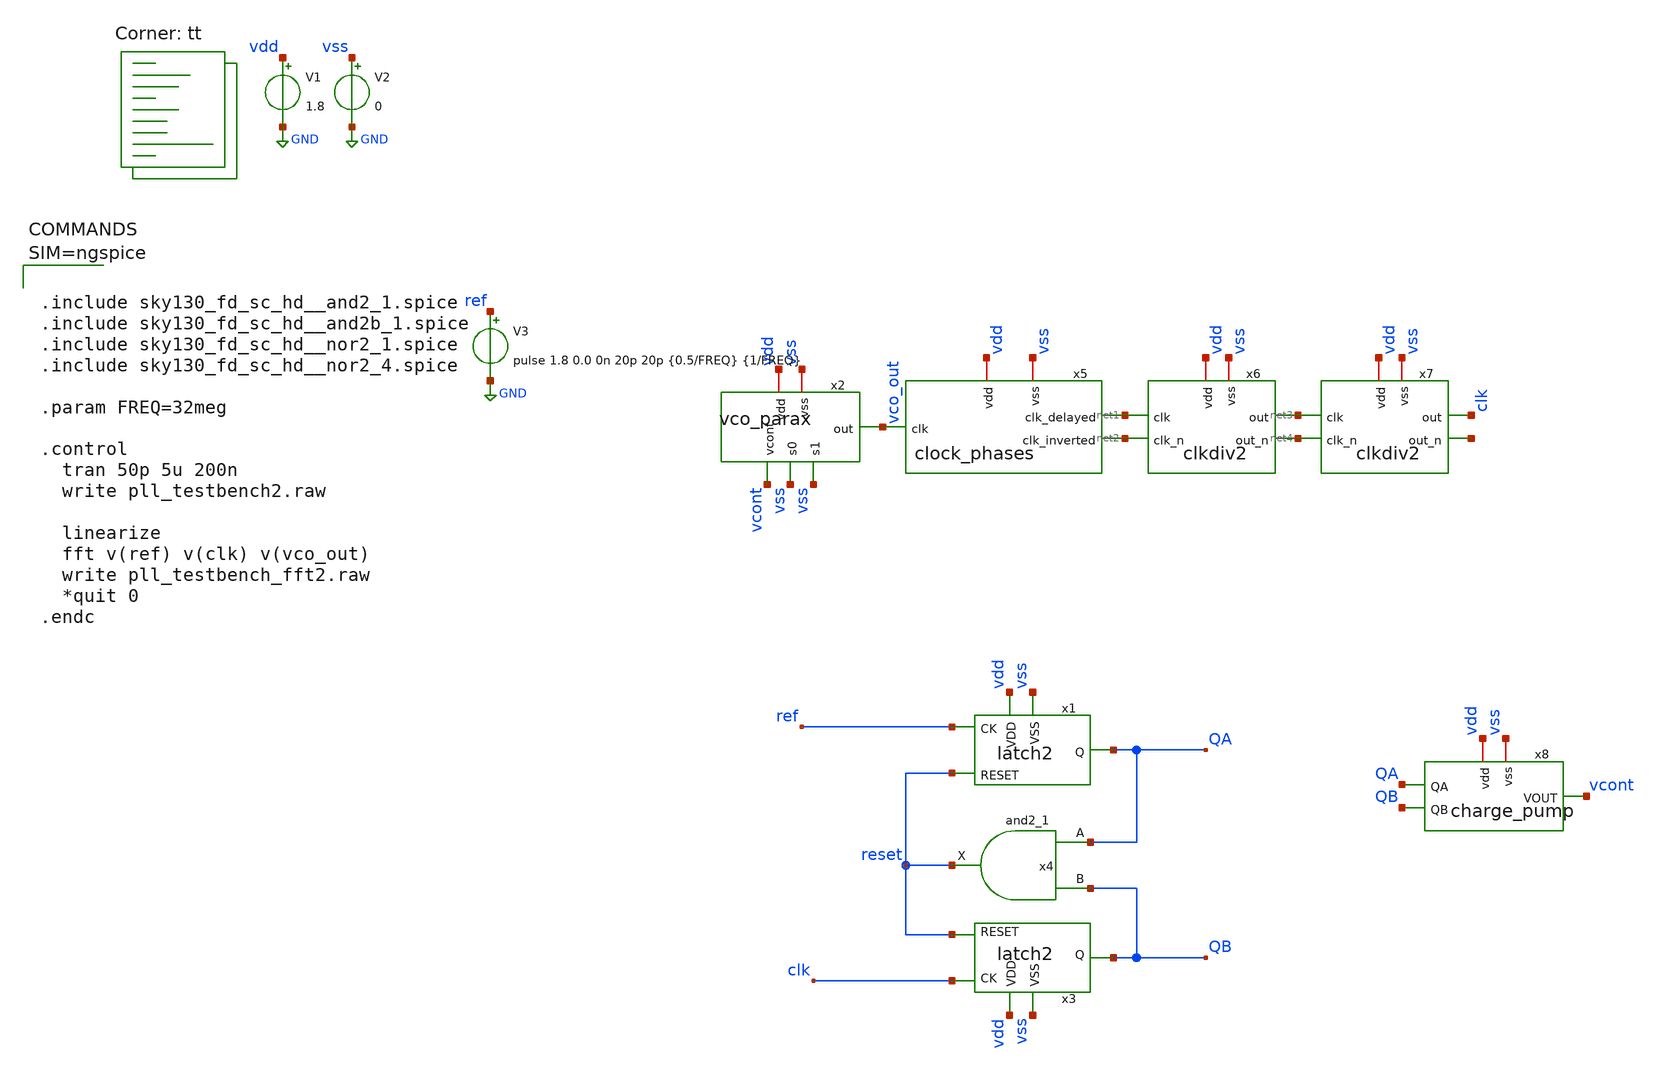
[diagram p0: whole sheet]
** sch_path: xschem/pll_testbench2.sch
**.subckt pll_testbench2
V1 vdd GND 1.8
V2 vss GND 0
x2 vdd vcont vss vss vco_out vss vco_parax
V3 ref GND pulse 1.8 0.0 0n 20p 20p {0.5/FREQ} {1/FREQ}
x1 ref QA reset vdd vss latch2
x3 clk QB reset vdd vss latch2
x4 QA QB vss vss vdd vdd reset sky130_fd_sc_hd__and2_1
x5 vdd net1 vco_out net2 vss clock_phases
x6 vdd vss net3 net4 net2 net1 clkdiv2
x7 vdd vss clk net5 net4 net3 clkdiv2
x8 vdd vss QA QB vcont charge_pump
**** begin user architecture code
.lib $::SKYWATER_MODELS/sky130.lib.spice tt



.include sky130_fd_sc_hd__and2_1.spice
.include sky130_fd_sc_hd__and2b_1.spice
.include sky130_fd_sc_hd__nor2_1.spice
.include sky130_fd_sc_hd__nor2_4.spice

.param FREQ=32meg

.control
  tran 50p 5u 200n
  write pll_testbench2.raw

  linearize
  fft v(ref) v(clk) v(vco_out)
  write pll_testbench_fft2.raw
  *quit 0
.endc



**** end user architecture code
**.ends

* expanding   symbol:  vco_parax.sym # of pins=6
** sym_path: xschem/vco.sym
.include [file normalize ../mag/vco.sim.spice]

* expanding   symbol:  latch2.sym # of pins=5
** sym_path: xschem/latch2.sym
** sch_path: xschem/latch2.sch
.subckt latch2 CK Q RESET VDD VSS
*.ipin RESET
*.ipin CK
*.opin Q
*.ipin VDD
*.ipin VSS
x1 net3 net2 VSS VSS VDD VDD net1 sky130_fd_sc_hd__nor2_1
x2 net1 RESET VSS VSS VDD VDD net2 sky130_fd_sc_hd__nor2_1
x3 CK Q VSS VSS VDD VDD net3 sky130_fd_sc_hd__nor2_1
x4 net3 net1 VSS VSS VDD VDD Q sky130_fd_sc_hd__nor2_4
.ends


* expanding   symbol:  clock_phases.sym # of pins=5
** sym_path: xschem/clock_phases.sym
** sch_path: xschem/clock_phases.sch
.subckt clock_phases vdd clk_delayed clk clk_inverted vss
*.ipin clk
*.iopin vdd
*.opin clk_delayed
*.opin clk_inverted
*.iopin vss
XM1 net2 clk vss vss sky130_fd_pr__nfet_01v8 L=0.15 W=1 nf=1 ad='int((nf+1)/2) * W/nf * 0.29' as='int((nf+2)/2) * W/nf * 0.29'
+ pd='2*int((nf+1)/2) * (W/nf + 0.29)' ps='2*int((nf+2)/2) * (W/nf + 0.29)' nrd='0.29 / W' nrs='0.29 / W'
+ sa=0 sb=0 sd=0 mult=1 m=1
XM2 clk_delayed net2 vdd vdd sky130_fd_pr__pfet_01v8 L=0.15 W=2 nf=1 ad='int((nf+1)/2) * W/nf * 0.29'
+ as='int((nf+2)/2) * W/nf * 0.29' pd='2*int((nf+1)/2) * (W/nf + 0.29)' ps='2*int((nf+2)/2) * (W/nf + 0.29)'
+ nrd='0.29 / W' nrs='0.29 / W' sa=0 sb=0 sd=0 mult=1 m=1
XM4 net2 clk vdd vdd sky130_fd_pr__pfet_01v8 L=0.15 W=2 nf=1 ad='int((nf+1)/2) * W/nf * 0.29' as='int((nf+2)/2) * W/nf * 0.29'
+ pd='2*int((nf+1)/2) * (W/nf + 0.29)' ps='2*int((nf+2)/2) * (W/nf + 0.29)' nrd='0.29 / W' nrs='0.29 / W'
+ sa=0 sb=0 sd=0 mult=1 m=1
XM8 clk_inverted net1 vdd vdd sky130_fd_pr__pfet_01v8 L=0.15 W=2 nf=1 ad='int((nf+1)/2) * W/nf * 0.29'
+ as='int((nf+2)/2) * W/nf * 0.29' pd='2*int((nf+1)/2) * (W/nf + 0.29)' ps='2*int((nf+2)/2) * (W/nf + 0.29)'
+ nrd='0.29 / W' nrs='0.29 / W' sa=0 sb=0 sd=0 mult=1 m=1
XM6 net1 vss clk vdd sky130_fd_pr__pfet_01v8 L=0.15 W=2 nf=1 ad='int((nf+1)/2) * W/nf * 0.29' as='int((nf+2)/2) * W/nf * 0.29'
+ pd='2*int((nf+1)/2) * (W/nf + 0.29)' ps='2*int((nf+2)/2) * (W/nf + 0.29)' nrd='0.29 / W' nrs='0.29 / W'
+ sa=0 sb=0 sd=0 mult=1 m=1
XM3 clk_delayed net2 vss vss sky130_fd_pr__nfet_01v8 L=0.15 W=1 nf=1 ad='int((nf+1)/2) * W/nf * 0.29'
+ as='int((nf+2)/2) * W/nf * 0.29' pd='2*int((nf+1)/2) * (W/nf + 0.29)' ps='2*int((nf+2)/2) * (W/nf + 0.29)'
+ nrd='0.29 / W' nrs='0.29 / W' sa=0 sb=0 sd=0 mult=1 m=1
XM7 clk_inverted net1 vss vss sky130_fd_pr__nfet_01v8 L=0.15 W=1 nf=1 ad='int((nf+1)/2) * W/nf * 0.29'
+ as='int((nf+2)/2) * W/nf * 0.29' pd='2*int((nf+1)/2) * (W/nf + 0.29)' ps='2*int((nf+2)/2) * (W/nf + 0.29)'
+ nrd='0.29 / W' nrs='0.29 / W' sa=0 sb=0 sd=0 mult=1 m=1
XM5 net1 vdd clk vss sky130_fd_pr__nfet_01v8 L=0.15 W=1 nf=1 ad='int((nf+1)/2) * W/nf * 0.29' as='int((nf+2)/2) * W/nf * 0.29'
+ pd='2*int((nf+1)/2) * (W/nf + 0.29)' ps='2*int((nf+2)/2) * (W/nf + 0.29)' nrd='0.29 / W' nrs='0.29 / W'
+ sa=0 sb=0 sd=0 mult=1 m=1
.ends


* expanding   symbol:  clkdiv2.sym # of pins=6
** sym_path: xschem/clkdiv2.sym
** sch_path: xschem/clkdiv2.sch
.subckt clkdiv2 vdd vss out out_n clk_n clk
*.iopin vdd
*.opin out
*.iopin vss
*.ipin clk
*.opin out_n
*.ipin clk_n
x2 vdd vss net1 net2 out_n out clk latch_parax
x3 vdd vss out_n out net2 net1 clk_n latch_parax
.ends


* expanding   symbol:  charge_pump.sym # of pins=5
** sym_path: xschem/charge_pump.sym
** sch_path: xschem/charge_pump.sch
.subckt charge_pump vdd vss QA QB VOUT
*.iopin vdd
*.iopin vss
*.ipin QA
*.opin VOUT
*.ipin QB
XM1 net2 QB net6 vss sky130_fd_pr__nfet_01v8 L=0.15 W=1 nf=1 ad='int((nf+1)/2) * W/nf * 0.29' as='int((nf+2)/2) * W/nf * 0.29'
+ pd='2*int((nf+1)/2) * (W/nf + 0.29)' ps='2*int((nf+2)/2) * (W/nf + 0.29)' nrd='0.29 / W' nrs='0.29 / W'
+ sa=0 sb=0 sd=0 mult=1 m=1
XM2 net2 net1 net4 vdd sky130_fd_pr__pfet_01v8 L=0.15 W=3 nf=1 ad='int((nf+1)/2) * W/nf * 0.29' as='int((nf+2)/2) * W/nf * 0.29'
+ pd='2*int((nf+1)/2) * (W/nf + 0.29)' ps='2*int((nf+2)/2) * (W/nf + 0.29)' nrd='0.29 / W' nrs='0.29 / W'
+ sa=0 sb=0 sd=0 mult=1 m=1
XM3 net1 QA vss vss sky130_fd_pr__nfet_01v8 L=0.15 W=1 nf=1 ad='int((nf+1)/2) * W/nf * 0.29' as='int((nf+2)/2) * W/nf * 0.29'
+ pd='2*int((nf+1)/2) * (W/nf + 0.29)' ps='2*int((nf+2)/2) * (W/nf + 0.29)' nrd='0.29 / W' nrs='0.29 / W'
+ sa=0 sb=0 sd=0 mult=1 m=1
XM4 net1 QA vdd vdd sky130_fd_pr__pfet_01v8 L=0.15 W=2 nf=1 ad='int((nf+1)/2) * W/nf * 0.29' as='int((nf+2)/2) * W/nf * 0.29'
+ pd='2*int((nf+1)/2) * (W/nf + 0.29)' ps='2*int((nf+2)/2) * (W/nf + 0.29)' nrd='0.29 / W' nrs='0.29 / W'
+ sa=0 sb=0 sd=0 mult=1 m=1
XC2 net7 GND sky130_fd_pr__cap_mim_m3_1 W=20 L=10 MF=1 m=1
R2 net7 net2 sky130_fd_pr__res_generic_l1 W=1 L=10 m=1
XC1 VOUT GND sky130_fd_pr__cap_mim_m3_1 W=10 L=10 MF=1 m=1
XM7 net4 net3 vdd vdd sky130_fd_pr__pfet_01v8 L=0.15 W=3 nf=1 ad='int((nf+1)/2) * W/nf * 0.29' as='int((nf+2)/2) * W/nf * 0.29'
+ pd='2*int((nf+1)/2) * (W/nf + 0.29)' ps='2*int((nf+2)/2) * (W/nf + 0.29)' nrd='0.29 / W' nrs='0.29 / W'
+ sa=0 sb=0 sd=0 mult=1 m=1
XM8 net3 net3 vdd vdd sky130_fd_pr__pfet_01v8 L=0.15 W=1 nf=1 ad='int((nf+1)/2) * W/nf * 0.29' as='int((nf+2)/2) * W/nf * 0.29'
+ pd='2*int((nf+1)/2) * (W/nf + 0.29)' ps='2*int((nf+2)/2) * (W/nf + 0.29)' nrd='0.29 / W' nrs='0.29 / W'
+ sa=0 sb=0 sd=0 mult=1 m=1
XM9 net6 net5 vss vss sky130_fd_pr__nfet_01v8 L=0.15 W=1 nf=1 ad='int((nf+1)/2) * W/nf * 0.29' as='int((nf+2)/2) * W/nf * 0.29'
+ pd='2*int((nf+1)/2) * (W/nf + 0.29)' ps='2*int((nf+2)/2) * (W/nf + 0.29)' nrd='0.29 / W' nrs='0.29 / W'
+ sa=0 sb=0 sd=0 mult=1 m=1
XM5 net5 net5 vss vss sky130_fd_pr__nfet_01v8 L=0.15 W=1 nf=1 ad='int((nf+1)/2) * W/nf * 0.29' as='int((nf+2)/2) * W/nf * 0.29'
+ pd='2*int((nf+1)/2) * (W/nf + 0.29)' ps='2*int((nf+2)/2) * (W/nf + 0.29)' nrd='0.29 / W' nrs='0.29 / W'
+ sa=0 sb=0 sd=0 mult=1 m=1
R3 vss net3 sky130_fd_pr__res_generic_l1 W=1 L=8.2 m=1
R4 net5 vdd sky130_fd_pr__res_generic_l1 W=1 L=16.4 m=1
R1 VOUT net2 sky130_fd_pr__res_generic_l1 W=1 L=8.2 m=1
.ends


* expanding   symbol:  latch_parax.sym # of pins=7
** sym_path: xschem/latch.sym
.include [file normalize ../mag/latch.sim.spice]
.GLOBAL GND
.end
